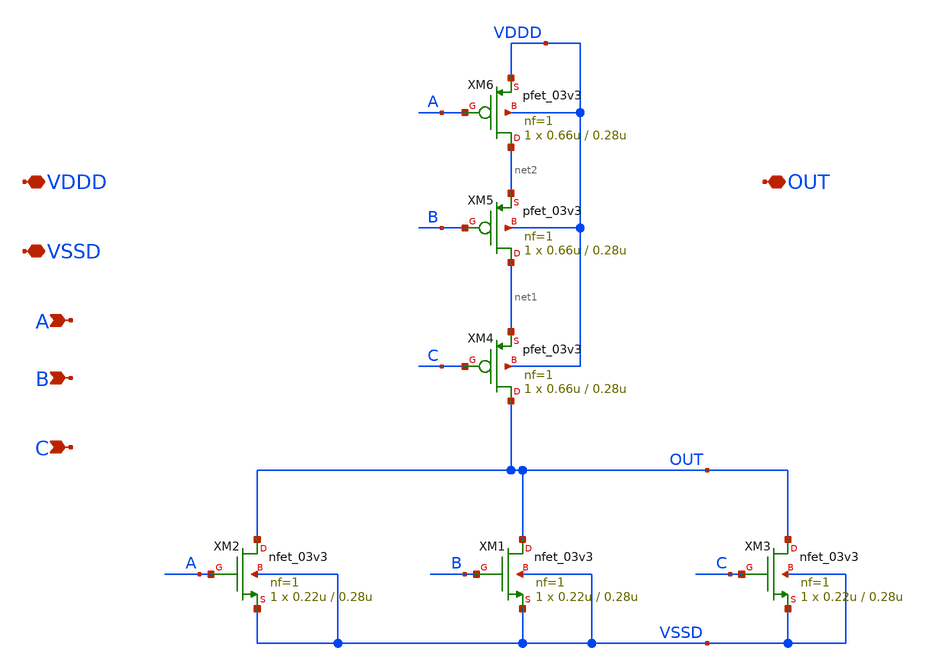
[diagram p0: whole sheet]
** sch_path: SAR_ADC/blocks/SAR_clock/clock_generator_nor_3_1x.sch
**.subckt clock_generator_nor_3_1x VDDD VSSD OUT A B C
*.iopin VDDD
*.iopin VSSD
*.iopin OUT
*.ipin A
*.ipin B
*.ipin C
XM1 OUT B VSSD VSSD nfet_03v3 L=0.28u W=0.22u nf=1 ad='int((nf+1)/2) * W/nf * 0.18u' as='int((nf+2)/2) * W/nf * 0.18u'
+ pd='2*int((nf+1)/2) * (W/nf + 0.18u)' ps='2*int((nf+2)/2) * (W/nf + 0.18u)' nrd='0.18u / W' nrs='0.18u / W'
+ sa=0 sb=0 sd=0 m=1
XM2 OUT A VSSD VSSD nfet_03v3 L=0.28u W=0.22u nf=1 ad='int((nf+1)/2) * W/nf * 0.18u' as='int((nf+2)/2) * W/nf * 0.18u'
+ pd='2*int((nf+1)/2) * (W/nf + 0.18u)' ps='2*int((nf+2)/2) * (W/nf + 0.18u)' nrd='0.18u / W' nrs='0.18u / W'
+ sa=0 sb=0 sd=0 m=1
XM3 OUT C VSSD VSSD nfet_03v3 L=0.28u W=0.22u nf=1 ad='int((nf+1)/2) * W/nf * 0.18u' as='int((nf+2)/2) * W/nf * 0.18u'
+ pd='2*int((nf+1)/2) * (W/nf + 0.18u)' ps='2*int((nf+2)/2) * (W/nf + 0.18u)' nrd='0.18u / W' nrs='0.18u / W'
+ sa=0 sb=0 sd=0 m=1
XM4 OUT C net1 VDDD pfet_03v3 L=0.28u W=0.66u nf=1 ad='int((nf+1)/2) * W/nf * 0.18u' as='int((nf+2)/2) * W/nf * 0.18u'
+ pd='2*int((nf+1)/2) * (W/nf + 0.18u)' ps='2*int((nf+2)/2) * (W/nf + 0.18u)' nrd='0.18u / W' nrs='0.18u / W'
+ sa=0 sb=0 sd=0 m=1
XM5 net1 B net2 VDDD pfet_03v3 L=0.28u W=0.66u nf=1 ad='int((nf+1)/2) * W/nf * 0.18u' as='int((nf+2)/2) * W/nf * 0.18u'
+ pd='2*int((nf+1)/2) * (W/nf + 0.18u)' ps='2*int((nf+2)/2) * (W/nf + 0.18u)' nrd='0.18u / W' nrs='0.18u / W'
+ sa=0 sb=0 sd=0 m=1
XM6 net2 A VDDD VDDD pfet_03v3 L=0.28u W=0.66u nf=1 ad='int((nf+1)/2) * W/nf * 0.18u' as='int((nf+2)/2) * W/nf * 0.18u'
+ pd='2*int((nf+1)/2) * (W/nf + 0.18u)' ps='2*int((nf+2)/2) * (W/nf + 0.18u)' nrd='0.18u / W' nrs='0.18u / W'
+ sa=0 sb=0 sd=0 m=1
**.ends
.end
